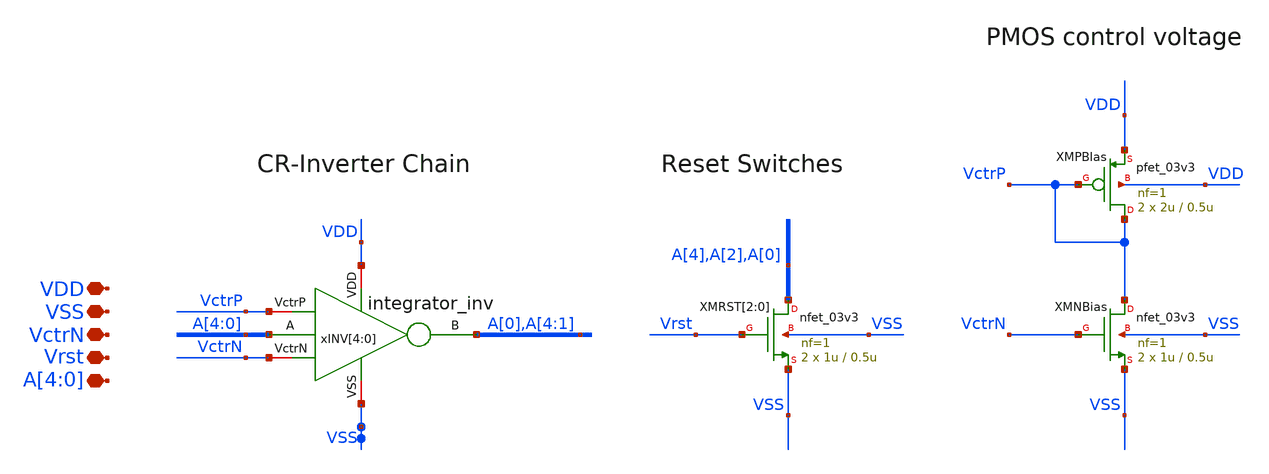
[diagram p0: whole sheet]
** sch_path: designs/ring_oscillator_pg/integrator/xschem/integrator_RO5St.sch
**.subckt integrator_RO5St VDD VctrN VSS Vrst A[4],A[3],A[2],A[1],A[0]
*.iopin VDD
*.iopin VctrN
*.iopin VSS
*.iopin Vrst
*.iopin A[4],A[3],A[2],A[1],A[0]
XMRST[2] A[4] Vrst VSS VSS nfet_03v3 L=0.5u W=1u nf=1 ad='int((nf+1)/2) * W/nf * 0.18u' as='int((nf+2)/2) * W/nf * 0.18u'
+ pd='2*int((nf+1)/2) * (W/nf + 0.18u)' ps='2*int((nf+2)/2) * (W/nf + 0.18u)' nrd='0.18u / W' nrs='0.18u / W'
+ sa=0 sb=0 sd=0 m=2
XMRST[1] A[2] Vrst VSS VSS nfet_03v3 L=0.5u W=1u nf=1 ad='int((nf+1)/2) * W/nf * 0.18u' as='int((nf+2)/2) * W/nf * 0.18u'
+ pd='2*int((nf+1)/2) * (W/nf + 0.18u)' ps='2*int((nf+2)/2) * (W/nf + 0.18u)' nrd='0.18u / W' nrs='0.18u / W'
+ sa=0 sb=0 sd=0 m=2
XMRST[0] A[0] Vrst VSS VSS nfet_03v3 L=0.5u W=1u nf=1 ad='int((nf+1)/2) * W/nf * 0.18u' as='int((nf+2)/2) * W/nf * 0.18u'
+ pd='2*int((nf+1)/2) * (W/nf + 0.18u)' ps='2*int((nf+2)/2) * (W/nf + 0.18u)' nrd='0.18u / W' nrs='0.18u / W'
+ sa=0 sb=0 sd=0 m=2
xINV[4] VDD A[0] A[4] VSS VctrP VctrN integrator_inv
xINV[3] VDD A[4] A[3] VSS VctrP VctrN integrator_inv
xINV[2] VDD A[3] A[2] VSS VctrP VctrN integrator_inv
xINV[1] VDD A[2] A[1] VSS VctrP VctrN integrator_inv
xINV[0] VDD A[1] A[0] VSS VctrP VctrN integrator_inv
XMNBias VctrP VctrN VSS VSS nfet_03v3 L=0.5u W=1u nf=1 ad='int((nf+1)/2) * W/nf * 0.18u' as='int((nf+2)/2) * W/nf * 0.18u'
+ pd='2*int((nf+1)/2) * (W/nf + 0.18u)' ps='2*int((nf+2)/2) * (W/nf + 0.18u)' nrd='0.18u / W' nrs='0.18u / W'
+ sa=0 sb=0 sd=0 m=2
XMPBIas VctrP VctrP VDD VDD pfet_03v3 L=0.5u W=2u nf=1 ad='int((nf+1)/2) * W/nf * 0.18u' as='int((nf+2)/2) * W/nf * 0.18u'
+ pd='2*int((nf+1)/2) * (W/nf + 0.18u)' ps='2*int((nf+2)/2) * (W/nf + 0.18u)' nrd='0.18u / W' nrs='0.18u / W'
+ sa=0 sb=0 sd=0 m=2
**.ends
.end
